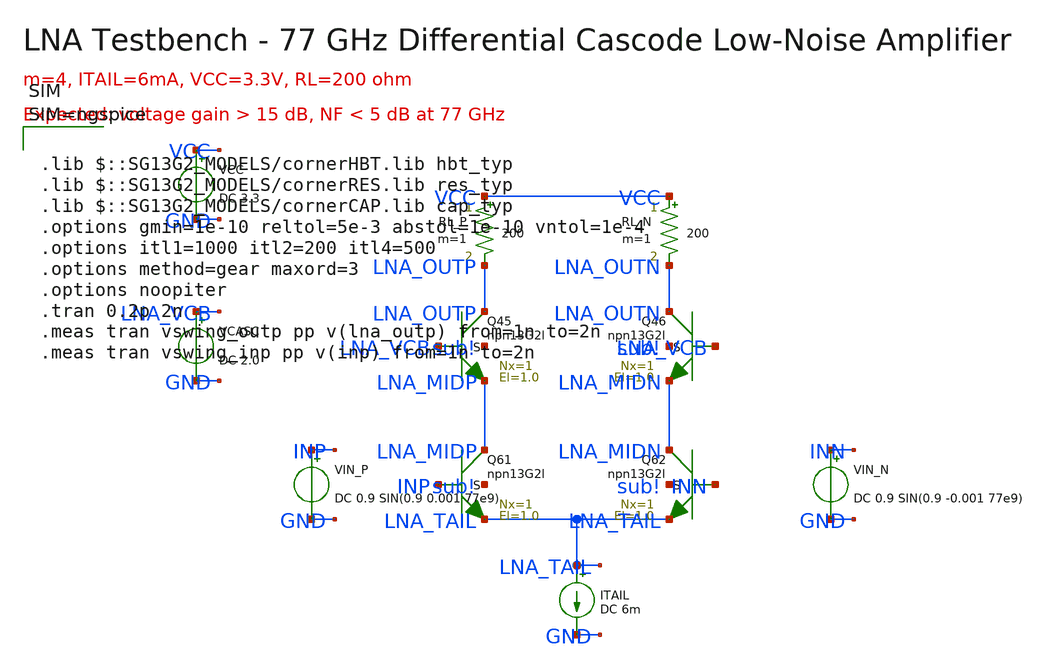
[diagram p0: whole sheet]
** sch_path: layout/testbenches/tb_lna.sch
**.subckt tb_lna
XQ61 LNA_MIDP INP LNA_TAIL sub! npn13G2l Nx=1 El=1.0 mm_ok=1
XQ62 LNA_MIDN INN LNA_TAIL sub! npn13G2l Nx=1 El=1.0 mm_ok=1
XQ45 LNA_OUTP LNA_VCB LNA_MIDP sub! npn13G2l Nx=1 El=1.0 mm_ok=1
XQ46 LNA_OUTN LNA_VCB LNA_MIDN sub! npn13G2l Nx=1 El=1.0 mm_ok=1
RL_P VCC LNA_OUTP 200 m=1
RL_N VCC LNA_OUTN 200 m=1
VCC VCC GND DC 3.3
ITAIL LNA_TAIL GND DC 6m
VIN_P INP GND DC 0.9 SIN(0.9 0.001 77e9)
VIN_N INN GND DC 0.9 SIN(0.9 -0.001 77e9)
VCASC LNA_VCB GND DC 2.0
**** begin user architecture code



.lib $::SG13G2_MODELS/cornerHBT.lib hbt_typ
.lib $::SG13G2_MODELS/cornerRES.lib res_typ
.lib $::SG13G2_MODELS/cornerCAP.lib cap_typ
.options gmin=1e-10 reltol=5e-3 abstol=1e-10 vntol=1e-4
.options itl1=1000 itl2=200 itl4=500
.options method=gear maxord=3
.options noopiter
.tran 0.2p 2n
.meas tran vswing_outp pp v(lna_outp) from=1n to=2n
.meas tran vswing_inp pp v(inp) from=1n to=2n



**** end user architecture code
**.ends
.end
